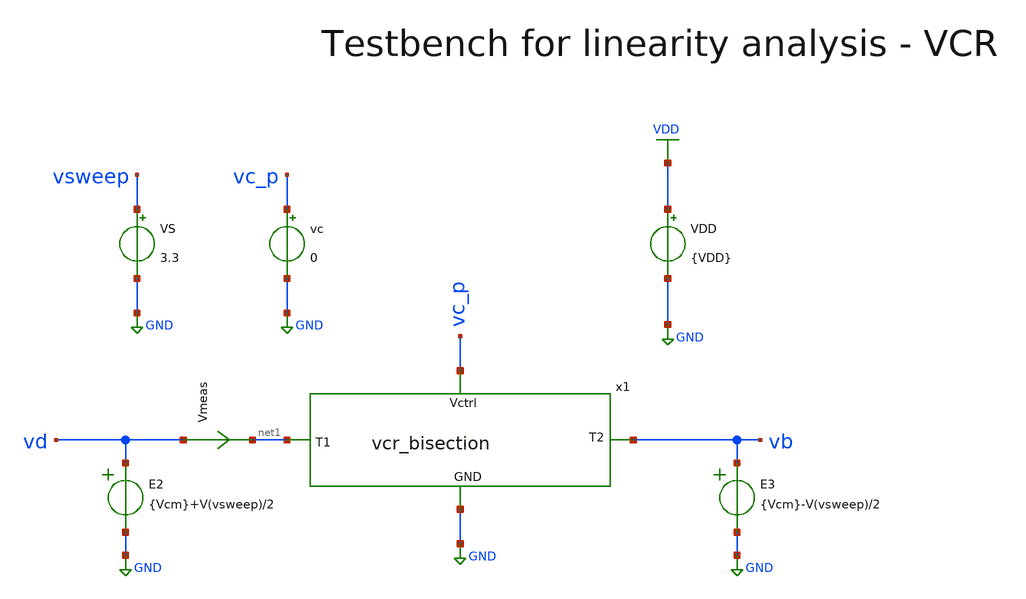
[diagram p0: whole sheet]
** sch_path: macros/heichips26_analog_project/testbenches/xschem/res_tb_linearity.sch
**.subckt res_tb_linearity
VDD VDD GND {VDD}
VS vsweep GND 3.3
Vmeas vd net1 0
.save i(vmeas)
E2 vd GND VOL=' {Vcm}+V(vsweep)/2 '
E3 vb GND VOL=' {Vcm}-V(vsweep)/2 '
vc vc_p GND 0
x1 vc_p net1 vb GND vcr_bisection
**** begin user architecture code

.lib cornerMOSlv.lib mos_tt
.lib cornerMOShv.lib mos_tt
.lib cornerRES.lib res_typ
.lib cornerDIO.lib dio_tt



* .include ../../../netlist/pex/inverter_magic_pex_3.spice
.param VDD=1.5
.csparam VDD=VDD
.param Vcm=VDD/2
.csparam Vcm=Vcm
.param temp=27
.options savecurrents klu method=gear reltol=1e-3 abstol=1e-15 gmin=1e-15
.control
let vcc = 0.0

save all
set appendwrite



repeat 5
  alter vc $&vcc

  * DC Sweep
  dc VS -1.5 1.5 1m
  remzerovec
  let vcc = vcc + 0.3
end
write @schname\.raw
set appendwrite

* Plotting
plot dc1.v(vsweep)/(dc1.v.x1.Vmeas#branch) dc2.v(vsweep)/(dc2.v.x1.Vmeas#branch)
+ dc3.v(vsweep)/(dc3.v.x1.Vmeas#branch) dc4.v(vsweep)/(dc4.v.x1.Vmeas#branch) dc5.v(vsweep)/(dc5.v.x1.Vmeas#branch) ylimit -10000k 10000k

plot dc1.v.x1.Vmeas#branch dc2.v.x1.Vmeas#branch dc3.v.x1.Vmeas#branch dc4.v.x1.Vmeas#branch
+ dc5.v.x1.Vmeas#branch

* Write Data
unset appendwrite
set wr_vecnames
set wr_singlescale
wrdata ../plot_simulations/data/@schname\.txt v(vc_p) dc1.v(vsweep)/(dc1.i(Vmeas))
+ dc2.v(vsweep)/(dc2.i(Vmeas)) dc3.v(vsweep)/(dc3.i(Vmeas)) dc4.v(vsweep)/(dc4.i(Vmeas)) dc5.v(vsweep)/(dc5.i(Vmeas))

write res_tb_linearity.raw

*quit
.endc


**** end user architecture code
**.ends
.GLOBAL GND
.GLOBAL VDD
.end
